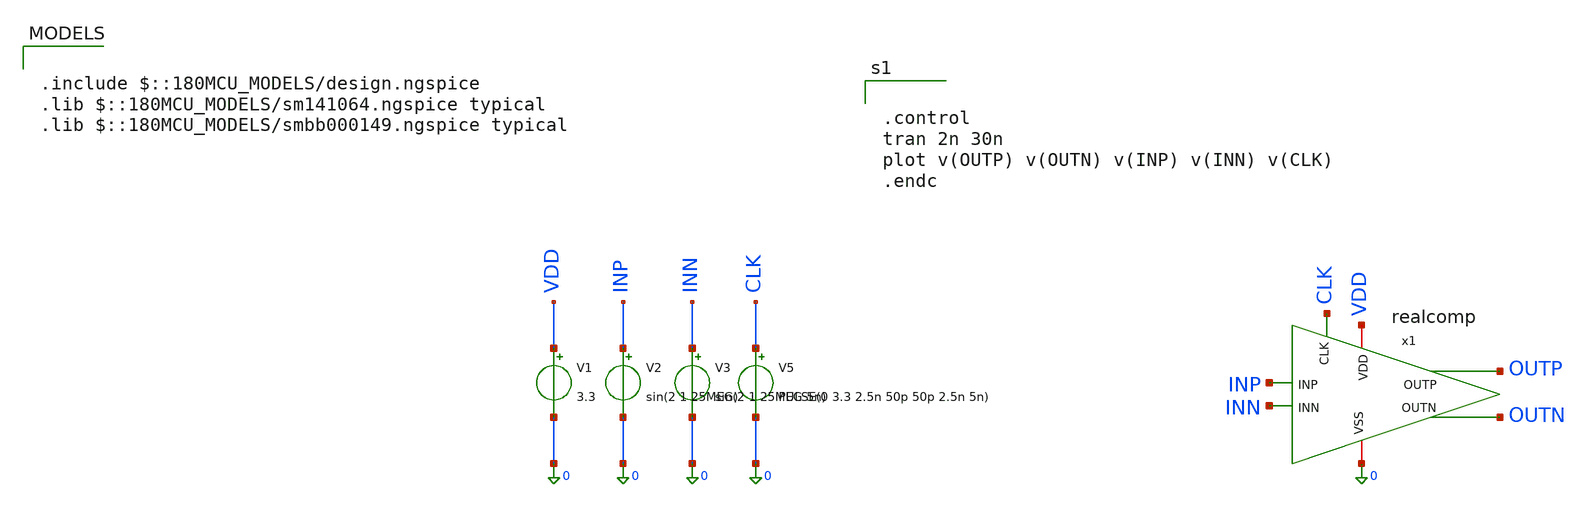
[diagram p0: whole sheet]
** sch_path: analog/blocks/Double_Tail_Comparator/realcomptest.sch
**.subckt realcomptest
V1 VDD 0 3.3
V2 INP 0 sin(2 1 25MEG)
V3 INN 0 sin(2 1 25MEG 5n)
V5 CLK 0 PULSE(0 3.3 2.5n 50p 50p 2.5n 5n)
x1 OUTN OUTP CLK 0 VDD INP INN realcomp
**** begin user architecture code

.include $::180MCU_MODELS/design.ngspice
.lib $::180MCU_MODELS/sm141064.ngspice typical
.lib $::180MCU_MODELS/smbb000149.ngspice typical



.control
tran 2n 30n
plot v(OUTP) v(OUTN) v(INP) v(INN) v(CLK)
.endc


**** end user architecture code
**.ends

* expanding   symbol:
*+  proj_branch/chipathon-2026-ti-adc/analog/blocks/Double_Tail_Comparator/realcomp.sym # of pins=7
** sym_path: analog/blocks/Double_Tail_Comparator/realcomp.sym
** sch_path: analog/blocks/Double_Tail_Comparator/realcomp.sch
.subckt realcomp OUTN OUTP CLK VSS VDD INP INN
*.ipin CLK
*.iopin VSS
*.iopin VDD
*.opin OUTP
*.opin OUTN
*.ipin INN
*.ipin INP
XM1 net1 INN net3 VSS nfet_03v3 L=0.28u W=1.4u nf=1 ad='int((nf+1)/2) * W/nf * 0.18u' as='int((nf+2)/2) * W/nf * 0.18u'
+ pd='2*int((nf+1)/2) * (W/nf + 0.18u)' ps='2*int((nf+2)/2) * (W/nf + 0.18u)' nrd='0.18u / W' nrs='0.18u / W'
+ sa=0 sb=0 sd=0 m=1
XM2 net2 INP net3 VSS nfet_03v3 L=0.28u W=1.4u nf=2 ad='int((nf+1)/2) * W/nf * 0.18u' as='int((nf+2)/2) * W/nf * 0.18u'
+ pd='2*int((nf+1)/2) * (W/nf + 0.18u)' ps='2*int((nf+2)/2) * (W/nf + 0.18u)' nrd='0.18u / W' nrs='0.18u / W'
+ sa=0 sb=0 sd=0 m=1
XM3 net3 CLK VSS VSS nfet_03v3 L=0.28u W=02.56u nf=2 ad='int((nf+1)/2) * W/nf * 0.18u' as='int((nf+2)/2) * W/nf * 0.18u'
+ pd='2*int((nf+1)/2) * (W/nf + 0.18u)' ps='2*int((nf+2)/2) * (W/nf + 0.18u)' nrd='0.18u / W' nrs='0.18u / W'
+ sa=0 sb=0 sd=0 m=1
XM4 OUTN OUTP net2 VSS nfet_03v3 L=0.28u W=0.71u nf=1 ad='int((nf+1)/2) * W/nf * 0.18u' as='int((nf+2)/2) * W/nf * 0.18u'
+ pd='2*int((nf+1)/2) * (W/nf + 0.18u)' ps='2*int((nf+2)/2) * (W/nf + 0.18u)' nrd='0.18u / W' nrs='0.18u / W'
+ sa=0 sb=0 sd=0 m=1
XM5 OUTP OUTN net1 VSS nfet_03v3 L=0.28u W=0.71u nf=1 ad='int((nf+1)/2) * W/nf * 0.18u' as='int((nf+2)/2) * W/nf * 0.18u'
+ pd='2*int((nf+1)/2) * (W/nf + 0.18u)' ps='2*int((nf+2)/2) * (W/nf + 0.18u)' nrd='0.18u / W' nrs='0.18u / W'
+ sa=0 sb=0 sd=0 m=1
XM6 OUTP CLK VDD VDD pfet_03v3 L=0.28u W=2.13u nf=3 ad='int((nf+1)/2) * W/nf * 0.18u' as='int((nf+2)/2) * W/nf * 0.18u'
+ pd='2*int((nf+1)/2) * (W/nf + 0.18u)' ps='2*int((nf+2)/2) * (W/nf + 0.18u)' nrd='0.18u / W' nrs='0.18u / W'
+ sa=0 sb=0 sd=0 m=1
XM7 OUTN OUTP VDD VDD pfet_03v3 L=0.28u W=1.42u nf=2 ad='int((nf+1)/2) * W/nf * 0.18u' as='int((nf+2)/2) * W/nf * 0.18u'
+ pd='2*int((nf+1)/2) * (W/nf + 0.18u)' ps='2*int((nf+2)/2) * (W/nf + 0.18u)' nrd='0.18u / W' nrs='0.18u / W'
+ sa=0 sb=0 sd=0 m=1
XM8 OUTN CLK VDD VDD pfet_03v3 L=0.28u W=2.13u nf=3 ad='int((nf+1)/2) * W/nf * 0.18u' as='int((nf+2)/2) * W/nf * 0.18u'
+ pd='2*int((nf+1)/2) * (W/nf + 0.18u)' ps='2*int((nf+2)/2) * (W/nf + 0.18u)' nrd='0.18u / W' nrs='0.18u / W'
+ sa=0 sb=0 sd=0 m=1
XM10 OUTP OUTN VDD VDD pfet_03v3 L=0.28u W=1.42u nf=2 ad='int((nf+1)/2) * W/nf * 0.18u' as='int((nf+2)/2) * W/nf * 0.18u'
+ pd='2*int((nf+1)/2) * (W/nf + 0.18u)' ps='2*int((nf+2)/2) * (W/nf + 0.18u)' nrd='0.18u / W' nrs='0.18u / W'
+ sa=0 sb=0 sd=0 m=1
XM9 net2 CLK net1 VDD pfet_03v3 L=0.28u W=2.88u nf=2 ad='int((nf+1)/2) * W/nf * 0.18u' as='int((nf+2)/2) * W/nf * 0.18u'
+ pd='2*int((nf+1)/2) * (W/nf + 0.18u)' ps='2*int((nf+2)/2) * (W/nf + 0.18u)' nrd='0.18u / W' nrs='0.18u / W'
+ sa=0 sb=0 sd=0 m=1
XM11 net1 INN net3 VSS nfet_03v3 L=0.28u W=1.4u nf=1 ad='int((nf+1)/2) * W/nf * 0.18u' as='int((nf+2)/2) * W/nf * 0.18u'
+ pd='2*int((nf+1)/2) * (W/nf + 0.18u)' ps='2*int((nf+2)/2) * (W/nf + 0.18u)' nrd='0.18u / W' nrs='0.18u / W'
+ sa=0 sb=0 sd=0 m=1
XM12 net2 INP net3 VSS nfet_03v3 L=0.28u W=1.4u nf=2 ad='int((nf+1)/2) * W/nf * 0.18u' as='int((nf+2)/2) * W/nf * 0.18u'
+ pd='2*int((nf+1)/2) * (W/nf + 0.18u)' ps='2*int((nf+2)/2) * (W/nf + 0.18u)' nrd='0.18u / W' nrs='0.18u / W'
+ sa=0 sb=0 sd=0 m=1
.ends

.end
